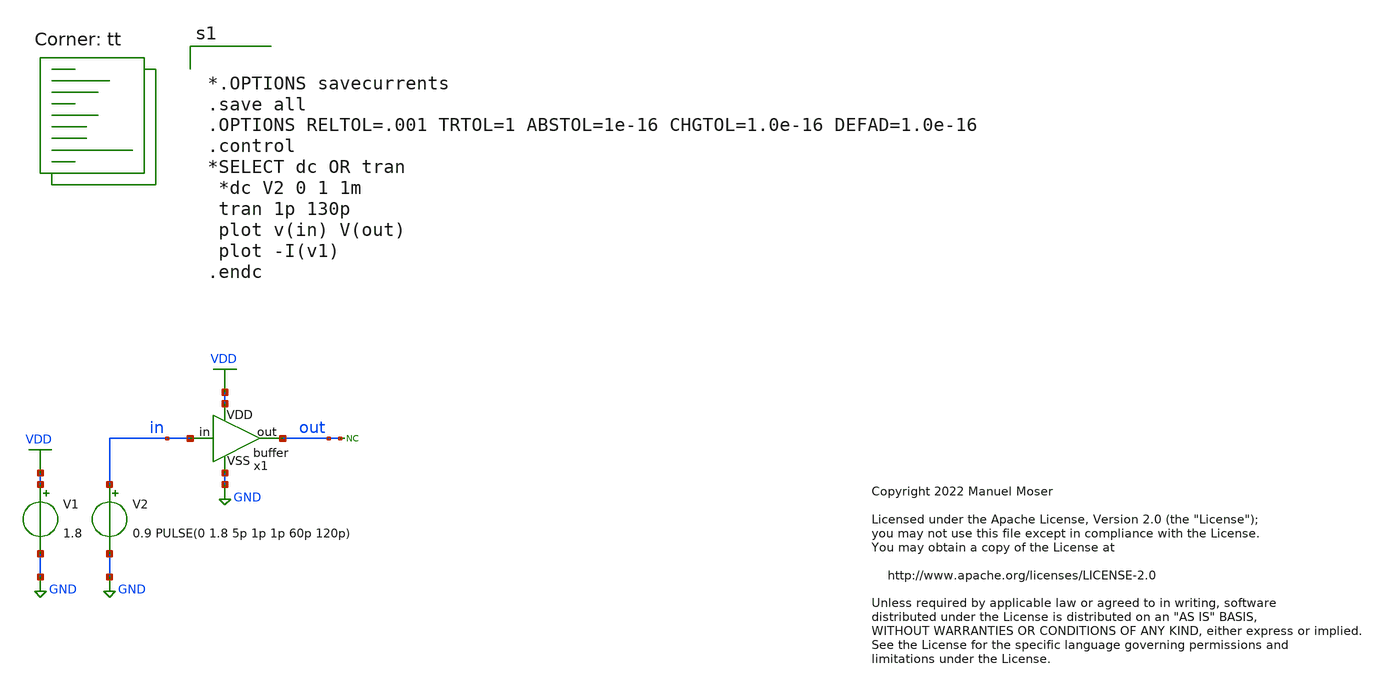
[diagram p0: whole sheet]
** sch_path: xschem/archive/buffer/buffer_tb.sch
* Copyright 2022 Manuel Moser
* Licensed under the Apache License, Version 2.0 (the "License");
**.subckt buffer_tb
V1 VDD GND 1.8
V2 in GND 0.9 PULSE(0 1.8 5p 1p 1p 60p 120p)
* noconn out
x1 VDD in out GND buffer
**** begin user architecture code


*.OPTIONS savecurrents
.save all
.OPTIONS RELTOL=.001 TRTOL=1 ABSTOL=1e-16 CHGTOL=1.0e-16 DEFAD=1.0e-16
.control
*SELECT dc OR tran
 *dc V2 0 1 1m
 tran 1p 130p
 plot v(in) V(out)
 plot -I(v1)
.endc


.lib $::SKYWATER_MODELS/sky130.lib.spice tt
**** end user architecture code
**.ends
.GLOBAL GND
.GLOBAL VDD
.end
